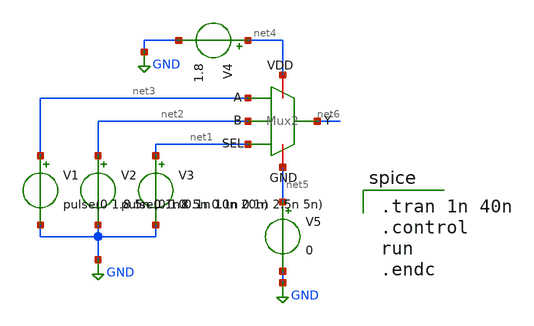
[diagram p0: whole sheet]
** sch_path: FinalProj/MUX2_Test.sch
**.subckt MUX2_Test
V1 net3 GND pulse(0 1.8 5n 0.1n 0.1n 10n 20n)
V2 net2 GND pulse(0 1.8 5n 0.1n 0.1n 2.5n 5n)
V3 net1 GND 0
V4 net4 GND 1.8
V5 net5 GND 0
x1 net4 net3 net5 net6 net2 net1 Mux2
**** begin user architecture code
 .lib $::SKYWATER_MODELS/sky130.lib.spice tt

.tran 1n 40n
.control
run
.endc

**** end user architecture code
**.ends

* expanding   symbol:  workspace/FinalProj/Mux2.sym # of pins=6
** sym_path: FinalProj/Mux2.sym
** sch_path: FinalProj/Mux2.sch
.subckt Mux2 VDD A GND Y B SEL
*.ipin A
*.ipin B
*.ipin SEL
*.iopin GND
*.opin Y
*.iopin VDD
x2 VDD net1 net3 A GND NAND
x4 VDD Y net2 net1 GND NAND
x3 VDD net2 SEL B GND NAND
x1 VDD SEL net3 GND Inv
.ends


* expanding   symbol:  workspace/FinalProj/NAND.sym # of pins=5
** sym_path: FinalProj/NAND.sym
** sch_path: FinalProj/NAND.sch
.subckt NAND VDD Y B A GND
*.ipin A
*.ipin B
*.iopin VDD
*.iopin GND
*.opin Y
XM1 Y B VDD VDD sky130_fd_pr__pfet_01v8 L=0.5 W=2 nf=1 ad='int((nf+1)/2) * W/nf * 0.29' as='int((nf+2)/2) * W/nf * 0.29'
+ pd='2*int((nf+1)/2) * (W/nf + 0.29)' ps='2*int((nf+2)/2) * (W/nf + 0.29)' nrd='0.29 / W' nrs='0.29 / W'
+ sa=0 sb=0 sd=0 mult=1 m=1
XM2 Y A VDD VDD sky130_fd_pr__pfet_01v8 L=0.5 W=2 nf=1 ad='int((nf+1)/2) * W/nf * 0.29' as='int((nf+2)/2) * W/nf * 0.29'
+ pd='2*int((nf+1)/2) * (W/nf + 0.29)' ps='2*int((nf+2)/2) * (W/nf + 0.29)' nrd='0.29 / W' nrs='0.29 / W'
+ sa=0 sb=0 sd=0 mult=1 m=1
XM3 Y B net1 GND sky130_fd_pr__nfet_01v8 L=0.5 W=2 nf=1 ad='int((nf+1)/2) * W/nf * 0.29' as='int((nf+2)/2) * W/nf * 0.29'
+ pd='2*int((nf+1)/2) * (W/nf + 0.29)' ps='2*int((nf+2)/2) * (W/nf + 0.29)' nrd='0.29 / W' nrs='0.29 / W'
+ sa=0 sb=0 sd=0 mult=1 m=1
XM4 net1 A GND GND sky130_fd_pr__nfet_01v8 L=0.5 W=2 nf=1 ad='int((nf+1)/2) * W/nf * 0.29' as='int((nf+2)/2) * W/nf * 0.29'
+ pd='2*int((nf+1)/2) * (W/nf + 0.29)' ps='2*int((nf+2)/2) * (W/nf + 0.29)' nrd='0.29 / W' nrs='0.29 / W'
+ sa=0 sb=0 sd=0 mult=1 m=1
.ends


* expanding   symbol:  workspace/FinalProj/Inv.sym # of pins=4
** sym_path: FinalProj/Inv.sym
** sch_path: FinalProj/Inv.sch
.subckt Inv VDD A Y GND
*.ipin A
*.iopin GND
*.iopin VDD
*.opin Y
XM1 Y A VDD VDD sky130_fd_pr__pfet_01v8 L=0.5 W=1 nf=1 ad='int((nf+1)/2) * W/nf * 0.29' as='int((nf+2)/2) * W/nf * 0.29'
+ pd='2*int((nf+1)/2) * (W/nf + 0.29)' ps='2*int((nf+2)/2) * (W/nf + 0.29)' nrd='0.29 / W' nrs='0.29 / W'
+ sa=0 sb=0 sd=0 mult=1 m=1
XM2 Y A GND GND sky130_fd_pr__nfet_01v8 L=0.5 W=0.5 nf=1 ad='int((nf+1)/2) * W/nf * 0.29' as='int((nf+2)/2) * W/nf * 0.29'
+ pd='2*int((nf+1)/2) * (W/nf + 0.29)' ps='2*int((nf+2)/2) * (W/nf + 0.29)' nrd='0.29 / W' nrs='0.29 / W'
+ sa=0 sb=0 sd=0 mult=1 m=1
.ends

.GLOBAL GND
.end
